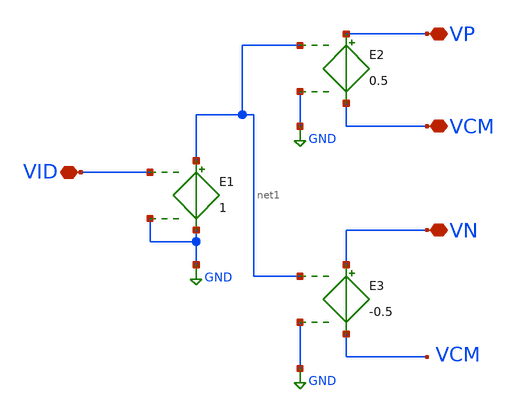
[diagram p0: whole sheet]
** sch_path: Designs/balun.sch
**.subckt balun VP VCM VN VID
*.iopin VP
*.iopin VCM
*.iopin VN
*.iopin VID
E2 VP VCM net1 GND 0.5
E3 VN VCM net1 GND -0.5
E1 net1 GND VID GND 1
**.ends
.GLOBAL GND
.end
